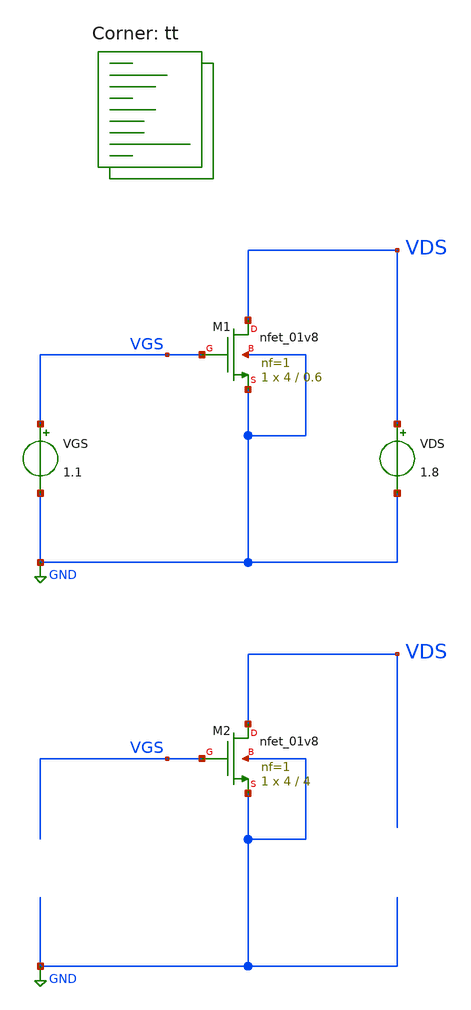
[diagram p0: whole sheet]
** sch_path: projects/bandgapref/xschem_ngspice/new_files/gm_id_check.sch
**.subckt gm_id_check
XM1 VDS VGS GND GND sky130_fd_pr__nfet_01v8 L=0.6 W=4 nf=1 ad='int((nf+1)/2) * W/nf * 0.29' as='int((nf+2)/2) * W/nf * 0.29'
+ pd='2*int((nf+1)/2) * (W/nf + 0.29)' ps='2*int((nf+2)/2) * (W/nf + 0.29)' nrd='0.29 / W' nrs='0.29 / W'
+ sa=0 sb=0 sd=0 mult=1 m=1
VGS VGS GND 1.1
VDS VDS GND 1.8
XM2 VDS VGS GND GND sky130_fd_pr__nfet_01v8 L=4 W=4 nf=1 ad='int((nf+1)/2) * W/nf * 0.29' as='int((nf+2)/2) * W/nf * 0.29'
+ pd='2*int((nf+1)/2) * (W/nf + 0.29)' ps='2*int((nf+2)/2) * (W/nf + 0.29)' nrd='0.29 / W' nrs='0.29 / W'
+ sa=0 sb=0 sd=0 mult=1 m=1
**** begin user architecture code
.lib $::SKYWATER_MODELS/sky130.lib.spice tt



.option method=gear
.option wnflag=1
.option savecurrents

.save @m.xm1.msky130_fd_pr__nfet_01v8[gm] @m.xm2.msky130_fd_pr__nfet_01v8[gm]

.control
  save all
  *  dc VGS 0 1.8 0.1 VDS 0 1.8 0.1
  dc VDS 0 1.8 0.001 VGS 0 1.8 0.1
  remzerovec
  write gm_id_check.raw
  set appendwrite
.endc



**** end user architecture code
**.ends
.GLOBAL GND
.end
